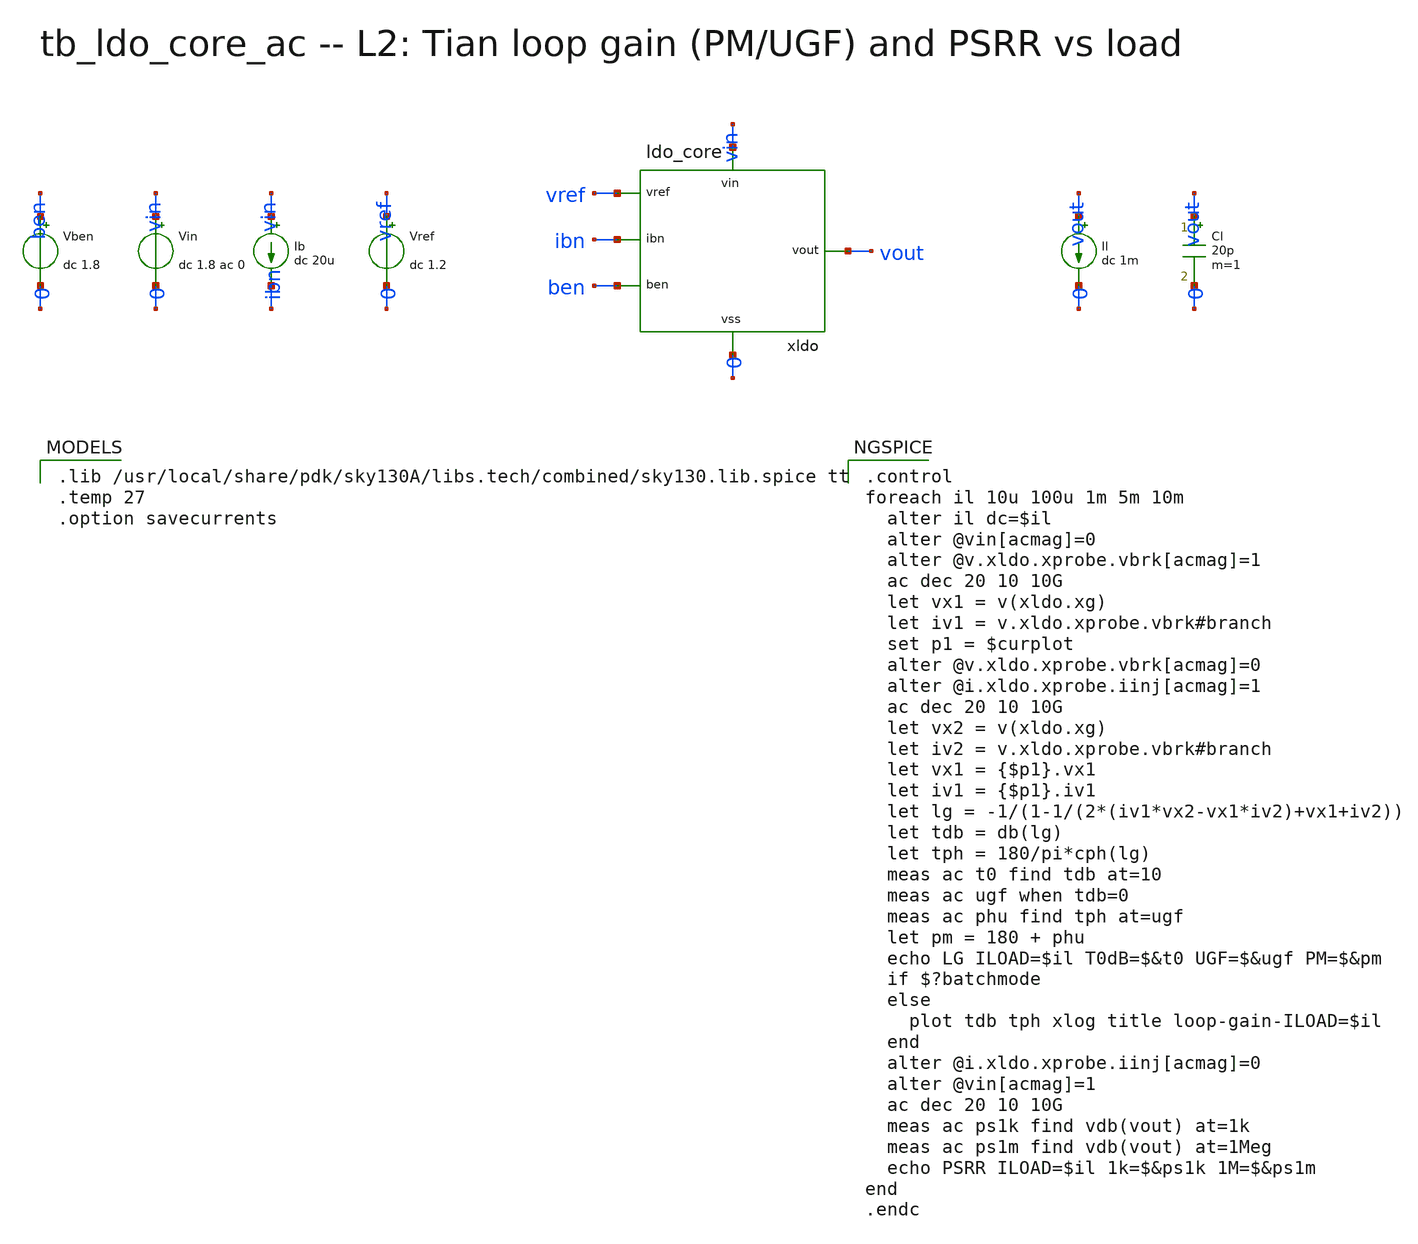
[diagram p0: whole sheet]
** sch_path: xschem/onetops_tb/tb_ldo_core_ac.sch
**.subckt tb_ldo_core_ac
Vin vin 0 dc 1.8 ac 0
Ib vin ibn dc 20u
Vben ben 0 dc 1.8
Vref vref 0 dc 1.2
xldo vref ibn ben vout vin 0 ldo_core
Il vout 0 dc 1m
Cl vout 0 20p m=1
**** begin user architecture code

.lib /usr/local/share/pdk/sky130A/libs.tech/combined/sky130.lib.spice tt
.temp 27
.option savecurrents


.control
foreach il 10u 100u 1m 5m 10m
  alter il dc=$il
  alter @vin[acmag]=0
  alter @v.xldo.xprobe.vbrk[acmag]=1
  ac dec 20 10 10G
  let vx1 = v(xldo.xg)
  let iv1 = v.xldo.xprobe.vbrk#branch
  set p1 = $curplot
  alter @v.xldo.xprobe.vbrk[acmag]=0
  alter @i.xldo.xprobe.iinj[acmag]=1
  ac dec 20 10 10G
  let vx2 = v(xldo.xg)
  let iv2 = v.xldo.xprobe.vbrk#branch
  let vx1 = {$p1}.vx1
  let iv1 = {$p1}.iv1
  let lg = -1/(1-1/(2*(iv1*vx2-vx1*iv2)+vx1+iv2))
  let tdb = db(lg)
  let tph = 180/pi*cph(lg)
  meas ac t0 find tdb at=10
  meas ac ugf when tdb=0
  meas ac phu find tph at=ugf
  let pm = 180 + phu
  echo LG ILOAD=$il T0dB=$&t0 UGF=$&ugf PM=$&pm
  if $?batchmode
  else
    plot tdb tph xlog title loop-gain-ILOAD=$il
  end
  alter @i.xldo.xprobe.iinj[acmag]=0
  alter @vin[acmag]=1
  ac dec 20 10 10G
  meas ac ps1k find vdb(vout) at=1k
  meas ac ps1m find vdb(vout) at=1Meg
  echo PSRR ILOAD=$il 1k=$&ps1k 1M=$&ps1m
end
.endc

**** end user architecture code
**.ends

* expanding   symbol:  onetops/ldo_core.sym # of pins=6
** sym_path: xschem/onetops/ldo_core.sym
** sch_path: xschem/onetops/ldo_core.sch
.subckt ldo_core vref ibn ben vout vin vss
*.ipin vref
*.ipin ibn
*.ipin ben
*.iopin vout
*.iopin vin
*.iopin vss
xbias ibn x i_pd i_tail i_bu i_dz vss bias_mirror
xboost ibn ben i_bu i_dz x vin vout vss tr_boost
xvset vref i_pd i_tail vset vin vset_gen
xfvf vset x vout fvf_core
xprobe x xg lg_probe
xpass xg vout vin pass_pmos
xcomp x vout comp_rc
.ends


* expanding   symbol:  onetops/bias_mirror.sym # of pins=7
** sym_path: xschem/onetops/bias_mirror.sym
** sch_path: xschem/onetops/bias_mirror.sch
.subckt bias_mirror ibn o_fvf o_pd o_tail o_bu o_dz vss
*.ipin ibn
*.opin o_fvf
*.opin o_pd
*.opin o_tail
*.opin o_bu
*.opin o_dz
*.iopin vss
XMN0 ibn ibn vss vss sky130_fd_pr__nfet_01v8 L=1 W=4 nf=1 ad='int((1 + 1)/2) * 4 / 1 * 0.29' as='int((1 + 2)/2) * 4 / 1 * 0.29'
+ pd='2*int((1 + 1)/2) * (4 / 1 + 0.29)' ps='2*int((1 + 2)/2) * (4 / 1 + 0.29)' nrd='0.29 / 4 ' nrs='0.29 / 4 '
+ sa=0 sb=0 sd=0 mult=1 m=1
XMN1 o_fvf ibn vss vss sky130_fd_pr__nfet_01v8 L=1 W=4 nf=1 ad='int((1 + 1)/2) * 4 / 1 * 0.29' as='int((1 + 2)/2) * 4 / 1 * 0.29'
+ pd='2*int((1 + 1)/2) * (4 / 1 + 0.29)' ps='2*int((1 + 2)/2) * (4 / 1 + 0.29)' nrd='0.29 / 4 ' nrs='0.29 / 4 '
+ sa=0 sb=0 sd=0 mult=1 m=1
XMN2 o_bu ibn vss vss sky130_fd_pr__nfet_01v8 L=1 W=4 nf=1 ad='int((1 + 1)/2) * 4 / 1 * 0.29' as='int((1 + 2)/2) * 4 / 1 * 0.29'
+ pd='2*int((1 + 1)/2) * (4 / 1 + 0.29)' ps='2*int((1 + 2)/2) * (4 / 1 + 0.29)' nrd='0.29 / 4 ' nrs='0.29 / 4 '
+ sa=0 sb=0 sd=0 mult=1 m=1
XMN3 o_pd ibn vss vss sky130_fd_pr__nfet_01v8 L=1 W=4 nf=1 ad='int((1 + 1)/2) * 4 / 1 * 0.29' as='int((1 + 2)/2) * 4 / 1 * 0.29'
+ pd='2*int((1 + 1)/2) * (4 / 1 + 0.29)' ps='2*int((1 + 2)/2) * (4 / 1 + 0.29)' nrd='0.29 / 4 ' nrs='0.29 / 4 '
+ sa=0 sb=0 sd=0 mult=1 m=1
XMN4 o_tail ibn vss vss sky130_fd_pr__nfet_01v8 L=1 W=4 nf=1 ad='int((1 + 1)/2) * 4 / 1 * 0.29' as='int((1 + 2)/2) * 4 / 1 * 0.29'
+ pd='2*int((1 + 1)/2) * (4 / 1 + 0.29)' ps='2*int((1 + 2)/2) * (4 / 1 + 0.29)' nrd='0.29 / 4 ' nrs='0.29 / 4 '
+ sa=0 sb=0 sd=0 mult=2 m=2
XMN5 o_dz ibn vss vss sky130_fd_pr__nfet_01v8 L=1 W=4 nf=1 ad='int((1 + 1)/2) * 4 / 1 * 0.29' as='int((1 + 2)/2) * 4 / 1 * 0.29'
+ pd='2*int((1 + 1)/2) * (4 / 1 + 0.29)' ps='2*int((1 + 2)/2) * (4 / 1 + 0.29)' nrd='0.29 / 4 ' nrs='0.29 / 4 '
+ sa=0 sb=0 sd=0 mult=1 m=1
.ends


* expanding   symbol:  onetops/tr_boost.sym # of pins=8
** sym_path: xschem/onetops/tr_boost.sym
** sch_path: xschem/onetops/tr_boost.sch
.subckt tr_boost ibn ben i_bu i_dz x vin vout vss
*.ipin ibn
*.ipin ben
*.iopin i_bu
*.iopin i_dz
*.iopin x
*.iopin vin
*.iopin vout
*.iopin vss
XMPB0 i_bu i_bu vin vin sky130_fd_pr__pfet_01v8_lvt L=0.5 W=40 nf=1 ad='int((1 + 1)/2) * 40 / 1 * 0.29'
+ as='int((1 + 2)/2) * 40 / 1 * 0.29' pd='2*int((1 + 1)/2) * (40 / 1 + 0.29)' ps='2*int((1 + 2)/2) * (40 / 1 + 0.29)'
+ nrd='0.29 / 40 ' nrs='0.29 / 40 ' sa=0 sb=0 sd=0 mult=1 m=1
Rbu i_bu gsu 1Meg m=1
Cbu vout gsu 0.5p m=1
XMPB1 i_dz gsu vin vin sky130_fd_pr__pfet_01v8_lvt L=0.5 W=20 nf=1 ad='int((1 + 1)/2) * 20 / 1 * 0.29'
+ as='int((1 + 2)/2) * 20 / 1 * 0.29' pd='2*int((1 + 1)/2) * (20 / 1 + 0.29)' ps='2*int((1 + 2)/2) * (20 / 1 + 0.29)'
+ nrd='0.29 / 20 ' nrs='0.29 / 20 ' sa=0 sb=0 sd=0 mult=1 m=1
XMNB0 i_dz i_dz vss vss sky130_fd_pr__nfet_01v8 L=0.5 W=2 nf=1 ad='int((1 + 1)/2) * 2 / 1 * 0.29' as='int((1 + 2)/2) * 2 / 1 * 0.29'
+ pd='2*int((1 + 1)/2) * (2 / 1 + 0.29)' ps='2*int((1 + 2)/2) * (2 / 1 + 0.29)' nrd='0.29 / 2 ' nrs='0.29 / 2 '
+ sa=0 sb=0 sd=0 mult=1 m=1
XMNB1 nsw i_dz vss vss sky130_fd_pr__nfet_01v8 L=0.5 W=2 nf=1 ad='int((1 + 1)/2) * 2 / 1 * 0.29' as='int((1 + 2)/2) * 2 / 1 * 0.29'
+ pd='2*int((1 + 1)/2) * (2 / 1 + 0.29)' ps='2*int((1 + 2)/2) * (2 / 1 + 0.29)' nrd='0.29 / 2 ' nrs='0.29 / 2 '
+ sa=0 sb=0 sd=0 mult=20 m=20
XMSW x ben nsw vss sky130_fd_pr__nfet_01v8 L=0.15 W=10 nf=1 ad='int((1 + 1)/2) * 10 / 1 * 0.29' as='int((1 + 2)/2) * 10 / 1 * 0.29'
+ pd='2*int((1 + 1)/2) * (10 / 1 + 0.29)' ps='2*int((1 + 2)/2) * (10 / 1 + 0.29)' nrd='0.29 / 10 ' nrs='0.29 / 10 '
+ sa=0 sb=0 sd=0 mult=1 m=1
Rbo ibn gso 1Meg m=1
Cbo vout gso 0.5p m=1
XMND vout gso vss vss sky130_fd_pr__nfet_01v8 L=1 W=4 nf=1 ad='int((1 + 1)/2) * 4 / 1 * 0.29' as='int((1 + 2)/2) * 4 / 1 * 0.29'
+ pd='2*int((1 + 1)/2) * (4 / 1 + 0.29)' ps='2*int((1 + 2)/2) * (4 / 1 + 0.29)' nrd='0.29 / 4 ' nrs='0.29 / 4 '
+ sa=0 sb=0 sd=0 mult=5 m=5
XMPDZ ndo i_bu vin vin sky130_fd_pr__pfet_01v8_lvt L=0.5 W=40 nf=1 ad='int((1 + 1)/2) * 40 / 1 * 0.29'
+ as='int((1 + 2)/2) * 40 / 1 * 0.29' pd='2*int((1 + 1)/2) * (40 / 1 + 0.29)' ps='2*int((1 + 2)/2) * (40 / 1 + 0.29)'
+ nrd='0.29 / 40 ' nrs='0.29 / 40 ' sa=0 sb=0 sd=0 mult=1 m=1
XMNS1 ndo gso vss vss sky130_fd_pr__nfet_01v8 L=1 W=2 nf=1 ad='int((1 + 1)/2) * 2 / 1 * 0.29' as='int((1 + 2)/2) * 2 / 1 * 0.29'
+ pd='2*int((1 + 1)/2) * (2 / 1 + 0.29)' ps='2*int((1 + 2)/2) * (2 / 1 + 0.29)' nrd='0.29 / 2 ' nrs='0.29 / 2 '
+ sa=0 sb=0 sd=0 mult=1 m=1
XMPO0 ndo ndo vin vin sky130_fd_pr__pfet_01v8 L=0.5 W=4 nf=1 ad='int((1 + 1)/2) * 4 / 1 * 0.29' as='int((1 + 2)/2) * 4 / 1 * 0.29'
+ pd='2*int((1 + 1)/2) * (4 / 1 + 0.29)' ps='2*int((1 + 2)/2) * (4 / 1 + 0.29)' nrd='0.29 / 4 ' nrs='0.29 / 4 '
+ sa=0 sb=0 sd=0 mult=1 m=1
XMPO1 psw ndo vin vin sky130_fd_pr__pfet_01v8 L=0.5 W=4 nf=1 ad='int((1 + 1)/2) * 4 / 1 * 0.29' as='int((1 + 2)/2) * 4 / 1 * 0.29'
+ pd='2*int((1 + 1)/2) * (4 / 1 + 0.29)' ps='2*int((1 + 2)/2) * (4 / 1 + 0.29)' nrd='0.29 / 4 ' nrs='0.29 / 4 '
+ sa=0 sb=0 sd=0 mult=20 m=20
XMPSW x benb psw vin sky130_fd_pr__pfet_01v8 L=0.15 W=20 nf=1 ad='int((1 + 1)/2) * 20 / 1 * 0.29' as='int((1 + 2)/2) * 20 / 1 * 0.29'
+ pd='2*int((1 + 1)/2) * (20 / 1 + 0.29)' ps='2*int((1 + 2)/2) * (20 / 1 + 0.29)' nrd='0.29 / 20 ' nrs='0.29 / 20 '
+ sa=0 sb=0 sd=0 mult=1 m=1
xinv ben benb vin vss inv
.ends


* expanding   symbol:  onetops/vset_gen.sym # of pins=5
** sym_path: xschem/onetops/vset_gen.sym
** sch_path: xschem/onetops/vset_gen.sch
.subckt vset_gen vref i_pd i_tail vset vin
*.ipin vref
*.opin vset
*.iopin i_pd
*.iopin i_tail
*.iopin vin
XMPD i_pd i_pd vin vin sky130_fd_pr__pfet_01v8_lvt L=2 W=10 nf=1 ad='int((1 + 1)/2) * 10 / 1 * 0.29'
+ as='int((1 + 2)/2) * 10 / 1 * 0.29' pd='2*int((1 + 1)/2) * (10 / 1 + 0.29)' ps='2*int((1 + 2)/2) * (10 / 1 + 0.29)'
+ nrd='0.29 / 10 ' nrs='0.29 / 10 ' sa=0 sb=0 sd=0 mult=1 m=1
XMPS vrep i_pd vin vin sky130_fd_pr__pfet_01v8_lvt L=2 W=10 nf=1 ad='int((1 + 1)/2) * 10 / 1 * 0.29'
+ as='int((1 + 2)/2) * 10 / 1 * 0.29' pd='2*int((1 + 1)/2) * (10 / 1 + 0.29)' ps='2*int((1 + 2)/2) * (10 / 1 + 0.29)'
+ nrd='0.29 / 10 ' nrs='0.29 / 10 ' sa=0 sb=0 sd=0 mult=1 m=1
XMR 0 vset vrep vrep sky130_fd_pr__pfet_01v8_lvt L=1 W=100 nf=1 ad='int((1 + 1)/2) * 100 / 1 * 0.29'
+ as='int((1 + 2)/2) * 100 / 1 * 0.29' pd='2*int((1 + 1)/2) * (100 / 1 + 0.29)' ps='2*int((1 + 2)/2) * (100 / 1 + 0.29)'
+ nrd='0.29 / 100 ' nrs='0.29 / 100 ' sa=0 sb=0 sd=0 mult=1 m=1
xota vref vrep i_tail vset vin ota5t
Cset vset 0 2p m=1
.ends


* expanding   symbol:  onetops/fvf_core.sym # of pins=3
** sym_path: xschem/onetops/fvf_core.sym
** sch_path: xschem/onetops/fvf_core.sch
.subckt fvf_core vset x vout
*.ipin vset
*.opin x
*.iopin vout
XMC x vset vout vout sky130_fd_pr__pfet_01v8_lvt L=1 W=100 nf=1 ad='int((1 + 1)/2) * 100 / 1 * 0.29'
+ as='int((1 + 2)/2) * 100 / 1 * 0.29' pd='2*int((1 + 1)/2) * (100 / 1 + 0.29)' ps='2*int((1 + 2)/2) * (100 / 1 + 0.29)'
+ nrd='0.29 / 100 ' nrs='0.29 / 100 ' sa=0 sb=0 sd=0 mult=1 m=1
.ends


* expanding   symbol:  onetops/lg_probe.sym # of pins=2
** sym_path: xschem/onetops/lg_probe.sym
** sch_path: xschem/onetops/lg_probe.sch
.subckt lg_probe drv lin
*.iopin drv
*.iopin lin
Vbrk lin drv dc 0 ac 0
Iinj 0 lin dc 0 ac 0
.ends


* expanding   symbol:  onetops/pass_pmos.sym # of pins=3
** sym_path: xschem/onetops/pass_pmos.sym
** sch_path: xschem/onetops/pass_pmos.sch
.subckt pass_pmos g vout vin
*.ipin g
*.iopin vin
*.iopin vout
XMP vout g vin vin sky130_fd_pr__pfet_01v8 L=0.35 W=10 nf=1 ad='int((1 + 1)/2) * 10 / 1 * 0.29' as='int((1 + 2)/2) * 10 / 1 * 0.29'
+ pd='2*int((1 + 1)/2) * (10 / 1 + 0.29)' ps='2*int((1 + 2)/2) * (10 / 1 + 0.29)' nrd='0.29 / 10 ' nrs='0.29 / 10 '
+ sa=0 sb=0 sd=0 mult=70 m=70
.ends


* expanding   symbol:  onetops/comp_rc.sym # of pins=2
** sym_path: xschem/onetops/comp_rc.sym
** sch_path: xschem/onetops/comp_rc.sch
.subckt comp_rc a b
*.iopin a
*.iopin b
Rz a n1 1 m=1
Cc n1 b 4p m=1
.ends


* expanding   symbol:  onetops/inv.sym # of pins=4
** sym_path: xschem/onetops/inv.sym
** sch_path: xschem/onetops/inv.sch
.subckt inv a y vdd vss
*.ipin a
*.opin y
*.iopin vdd
*.iopin vss
XMP1 y a vdd vdd sky130_fd_pr__pfet_01v8 L=0.15 W=2 nf=1 ad='int((1 + 1)/2) * 2 / 1 * 0.29' as='int((1 + 2)/2) * 2 / 1 * 0.29'
+ pd='2*int((1 + 1)/2) * (2 / 1 + 0.29)' ps='2*int((1 + 2)/2) * (2 / 1 + 0.29)' nrd='0.29 / 2 ' nrs='0.29 / 2 '
+ sa=0 sb=0 sd=0 mult=1 m=1
XMN1 y a vss vss sky130_fd_pr__nfet_01v8 L=0.15 W=1 nf=1 ad='int((1 + 1)/2) * 1 / 1 * 0.29' as='int((1 + 2)/2) * 1 / 1 * 0.29'
+ pd='2*int((1 + 1)/2) * (1 / 1 + 0.29)' ps='2*int((1 + 2)/2) * (1 / 1 + 0.29)' nrd='0.29 / 1 ' nrs='0.29 / 1 '
+ sa=0 sb=0 sd=0 mult=1 m=1
.ends


* expanding   symbol:  onetops/ota5t.sym # of pins=5
** sym_path: xschem/onetops/ota5t.sym
** sch_path: xschem/onetops/ota5t.sch
.subckt ota5t inp inn tail out vdd
*.ipin inp
*.ipin inn
*.opin out
*.iopin tail
*.iopin vdd
XMP1 nd nd vdd vdd sky130_fd_pr__pfet_01v8_lvt L=2 W=20 nf=1 ad='int((1 + 1)/2) * 20 / 1 * 0.29' as='int((1 + 2)/2) * 20 / 1 * 0.29'
+ pd='2*int((1 + 1)/2) * (20 / 1 + 0.29)' ps='2*int((1 + 2)/2) * (20 / 1 + 0.29)' nrd='0.29 / 20 ' nrs='0.29 / 20 '
+ sa=0 sb=0 sd=0 mult=1 m=1
XMP2 out nd vdd vdd sky130_fd_pr__pfet_01v8_lvt L=2 W=20 nf=1 ad='int((1 + 1)/2) * 20 / 1 * 0.29' as='int((1 + 2)/2) * 20 / 1 * 0.29'
+ pd='2*int((1 + 1)/2) * (20 / 1 + 0.29)' ps='2*int((1 + 2)/2) * (20 / 1 + 0.29)' nrd='0.29 / 20 ' nrs='0.29 / 20 '
+ sa=0 sb=0 sd=0 mult=1 m=1
XMN1 nd inp tail 0 sky130_fd_pr__nfet_01v8 L=1 W=5 nf=1 ad='int((1 + 1)/2) * 5 / 1 * 0.29' as='int((1 + 2)/2) * 5 / 1 * 0.29'
+ pd='2*int((1 + 1)/2) * (5 / 1 + 0.29)' ps='2*int((1 + 2)/2) * (5 / 1 + 0.29)' nrd='0.29 / 5 ' nrs='0.29 / 5 '
+ sa=0 sb=0 sd=0 mult=1 m=1
XMN2 out inn tail 0 sky130_fd_pr__nfet_01v8 L=1 W=5 nf=1 ad='int((1 + 1)/2) * 5 / 1 * 0.29' as='int((1 + 2)/2) * 5 / 1 * 0.29'
+ pd='2*int((1 + 1)/2) * (5 / 1 + 0.29)' ps='2*int((1 + 2)/2) * (5 / 1 + 0.29)' nrd='0.29 / 5 ' nrs='0.29 / 5 '
+ sa=0 sb=0 sd=0 mult=1 m=1
.ends

.end
